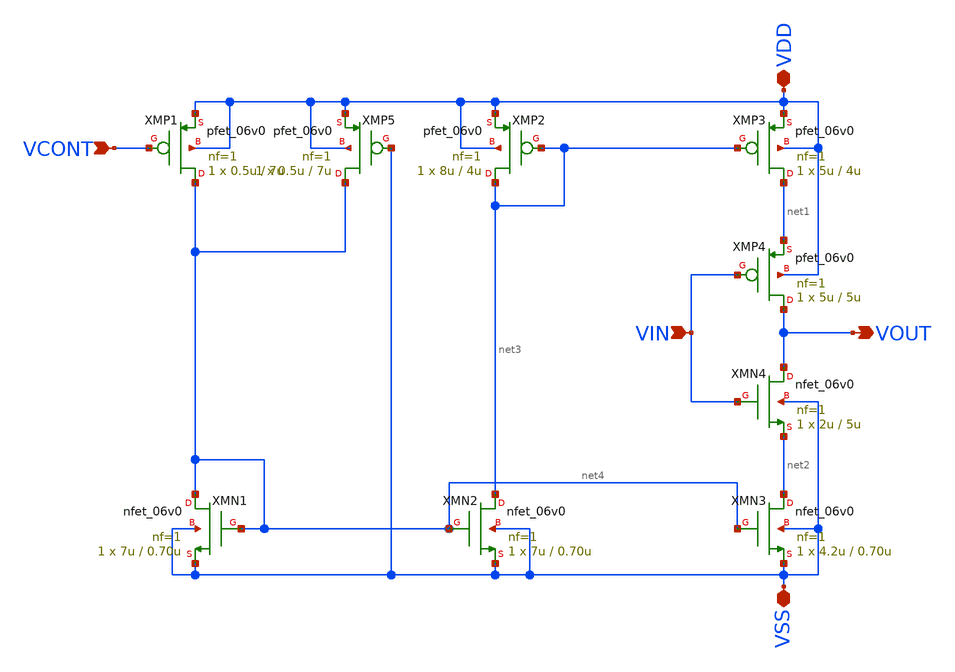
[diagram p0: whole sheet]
** sch_path: xschem/vco/stage_v3p1_GF180-5V.sch
**.subckt stage_v3p1_GF180-5V VIN VOUT VDD VSS VCONT
*.ipin VIN
*.opin VOUT
*.iopin VDD
*.iopin VSS
*.ipin VCONT
XMP3 net1 net3 VDD VDD pfet_06v0 L=4u W=5u nf=1 ad='int((nf+1)/2) * W/nf * 0.18u' as='int((nf+2)/2) * W/nf * 0.18u'
+ pd='2*int((nf+1)/2) * (W/nf + 0.18u)' ps='2*int((nf+2)/2) * (W/nf + 0.18u)' nrd='0.18u / W' nrs='0.18u / W'
+ sa=0 sb=0 sd=0 m=1
XMP4 VOUT VIN net1 VDD pfet_06v0 L=5u W=5u nf=1 ad='int((nf+1)/2) * W/nf * 0.18u' as='int((nf+2)/2) * W/nf * 0.18u'
+ pd='2*int((nf+1)/2) * (W/nf + 0.18u)' ps='2*int((nf+2)/2) * (W/nf + 0.18u)' nrd='0.18u / W' nrs='0.18u / W'
+ sa=0 sb=0 sd=0 m=1
XMP2 net3 net3 VDD VDD pfet_06v0 L=4u W=8u nf=1 ad='int((nf+1)/2) * W/nf * 0.18u' as='int((nf+2)/2) * W/nf * 0.18u'
+ pd='2*int((nf+1)/2) * (W/nf + 0.18u)' ps='2*int((nf+2)/2) * (W/nf + 0.18u)' nrd='0.18u / W' nrs='0.18u / W'
+ sa=0 sb=0 sd=0 m=1
XMP1 net4 VCONT VDD VDD pfet_06v0 L=7u W=0.5u nf=1 ad='int((nf+1)/2) * W/nf * 0.18u' as='int((nf+2)/2) * W/nf * 0.18u'
+ pd='2*int((nf+1)/2) * (W/nf + 0.18u)' ps='2*int((nf+2)/2) * (W/nf + 0.18u)' nrd='0.18u / W' nrs='0.18u / W'
+ sa=0 sb=0 sd=0 m=1
XMN2 net3 net4 VSS VSS nfet_06v0 L=0.70u W=7u nf=1 ad='int((nf+1)/2) * W/nf * 0.18u' as='int((nf+2)/2) * W/nf * 0.18u'
+ pd='2*int((nf+1)/2) * (W/nf + 0.18u)' ps='2*int((nf+2)/2) * (W/nf + 0.18u)' nrd='0.18u / W' nrs='0.18u / W'
+ sa=0 sb=0 sd=0 m=1
XMN3 net2 net4 VSS VSS nfet_06v0 L=0.70u W=4.2u nf=1 ad='int((nf+1)/2) * W/nf * 0.18u' as='int((nf+2)/2) * W/nf * 0.18u'
+ pd='2*int((nf+1)/2) * (W/nf + 0.18u)' ps='2*int((nf+2)/2) * (W/nf + 0.18u)' nrd='0.18u / W' nrs='0.18u / W'
+ sa=0 sb=0 sd=0 m=1
XMN4 VOUT VIN net2 VSS nfet_06v0 L=5u W=2u nf=1 ad='int((nf+1)/2) * W/nf * 0.18u' as='int((nf+2)/2) * W/nf * 0.18u'
+ pd='2*int((nf+1)/2) * (W/nf + 0.18u)' ps='2*int((nf+2)/2) * (W/nf + 0.18u)' nrd='0.18u / W' nrs='0.18u / W'
+ sa=0 sb=0 sd=0 m=1
XMN1 net4 net4 VSS VSS nfet_06v0 L=0.70u W=7u nf=1 ad='int((nf+1)/2) * W/nf * 0.18u' as='int((nf+2)/2) * W/nf * 0.18u'
+ pd='2*int((nf+1)/2) * (W/nf + 0.18u)' ps='2*int((nf+2)/2) * (W/nf + 0.18u)' nrd='0.18u / W' nrs='0.18u / W'
+ sa=0 sb=0 sd=0 m=1
XMP5 net4 VSS VDD VDD pfet_06v0 L=7u W=0.5u nf=1 ad='int((nf+1)/2) * W/nf * 0.18u' as='int((nf+2)/2) * W/nf * 0.18u'
+ pd='2*int((nf+1)/2) * (W/nf + 0.18u)' ps='2*int((nf+2)/2) * (W/nf + 0.18u)' nrd='0.18u / W' nrs='0.18u / W'
+ sa=0 sb=0 sd=0 m=1
**.ends
.end
